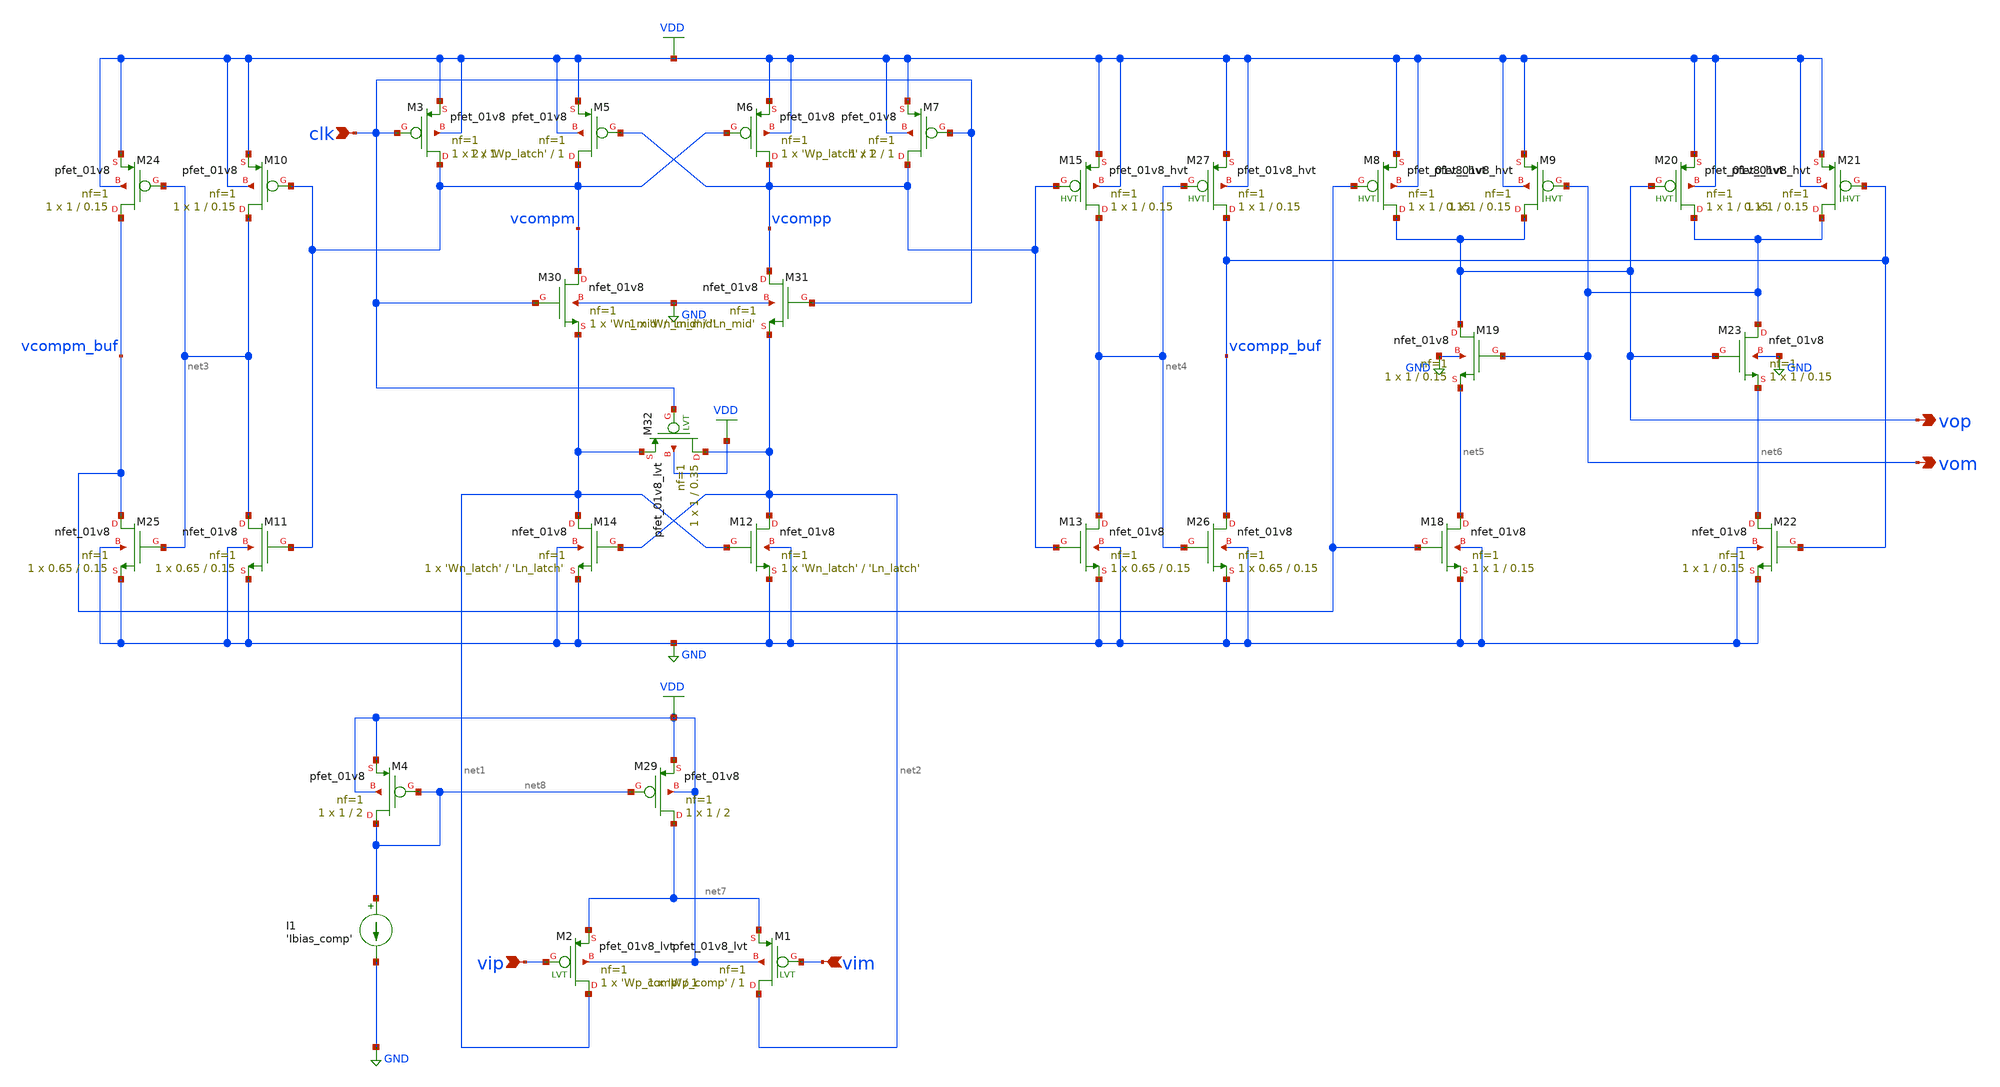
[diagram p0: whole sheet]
** sch_path: designs/latched_comparator_folded.sch
**.subckt latched_comparator_folded vip vim vop vom clk
*.ipin vip
*.ipin vim
*.opin vop
*.opin vom
*.ipin clk
XM5 vcompm vcompp VDD VDD sky130_fd_pr__pfet_01v8 L=1 W='Wp_latch' nf=1 ad='int((nf+1)/2) * W/nf * 0.29'
+ as='int((nf+2)/2) * W/nf * 0.29' pd='2*int((nf+1)/2) * (W/nf + 0.29)' ps='2*int((nf+2)/2) * (W/nf + 0.29)'
+ nrd='0.29 / W' nrs='0.29 / W' sa=0 sb=0 sd=0 mult=1 m=1
XM10 net3 vcompm VDD VDD sky130_fd_pr__pfet_01v8 L=0.15 W=1 nf=1 ad='int((nf+1)/2) * W/nf * 0.29' as='int((nf+2)/2) * W/nf * 0.29'
+ pd='2*int((nf+1)/2) * (W/nf + 0.29)' ps='2*int((nf+2)/2) * (W/nf + 0.29)' nrd='0.29 / W' nrs='0.29 / W'
+ sa=0 sb=0 sd=0 mult=1 m=1
XM11 net3 vcompm GND GND sky130_fd_pr__nfet_01v8 L=0.15 W=0.65 nf=1 ad='int((nf+1)/2) * W/nf * 0.29'
+ as='int((nf+2)/2) * W/nf * 0.29' pd='2*int((nf+1)/2) * (W/nf + 0.29)' ps='2*int((nf+2)/2) * (W/nf + 0.29)'
+ nrd='0.29 / W' nrs='0.29 / W' sa=0 sb=0 sd=0 mult=1 m=1
XM13 net4 vcompp GND GND sky130_fd_pr__nfet_01v8 L=0.15 W=0.65 nf=1 ad='int((nf+1)/2) * W/nf * 0.29'
+ as='int((nf+2)/2) * W/nf * 0.29' pd='2*int((nf+1)/2) * (W/nf + 0.29)' ps='2*int((nf+2)/2) * (W/nf + 0.29)'
+ nrd='0.29 / W' nrs='0.29 / W' sa=0 sb=0 sd=0 mult=1 m=1
XM15 net4 vcompp VDD VDD sky130_fd_pr__pfet_01v8_hvt L=0.15 W=1 nf=1 ad='int((nf+1)/2) * W/nf * 0.29'
+ as='int((nf+2)/2) * W/nf * 0.29' pd='2*int((nf+1)/2) * (W/nf + 0.29)' ps='2*int((nf+2)/2) * (W/nf + 0.29)'
+ nrd='0.29 / W' nrs='0.29 / W' sa=0 sb=0 sd=0 mult=1 m=1
XM6 vcompp vcompm VDD VDD sky130_fd_pr__pfet_01v8 L=1 W='Wp_latch' nf=1 ad='int((nf+1)/2) * W/nf * 0.29'
+ as='int((nf+2)/2) * W/nf * 0.29' pd='2*int((nf+1)/2) * (W/nf + 0.29)' ps='2*int((nf+2)/2) * (W/nf + 0.29)'
+ nrd='0.29 / W' nrs='0.29 / W' sa=0 sb=0 sd=0 mult=1 m=1
XM12 net2 net1 GND GND sky130_fd_pr__nfet_01v8 L='Ln_latch' W='Wn_latch' nf=1 ad='int((nf+1)/2) * W/nf * 0.29'
+ as='int((nf+2)/2) * W/nf * 0.29' pd='2*int((nf+1)/2) * (W/nf + 0.29)' ps='2*int((nf+2)/2) * (W/nf + 0.29)'
+ nrd='0.29 / W' nrs='0.29 / W' sa=0 sb=0 sd=0 mult=1 m=1
XM14 net1 net2 GND GND sky130_fd_pr__nfet_01v8 L='Ln_latch' W='Wn_latch' nf=1 ad='int((nf+1)/2) * W/nf * 0.29'
+ as='int((nf+2)/2) * W/nf * 0.29' pd='2*int((nf+1)/2) * (W/nf + 0.29)' ps='2*int((nf+2)/2) * (W/nf + 0.29)'
+ nrd='0.29 / W' nrs='0.29 / W' sa=0 sb=0 sd=0 mult=1 m=1
XM3 vcompm clk VDD VDD sky130_fd_pr__pfet_01v8 L=1 W=2 nf=1 ad='int((nf+1)/2) * W/nf * 0.29' as='int((nf+2)/2) * W/nf * 0.29'
+ pd='2*int((nf+1)/2) * (W/nf + 0.29)' ps='2*int((nf+2)/2) * (W/nf + 0.29)' nrd='0.29 / W' nrs='0.29 / W'
+ sa=0 sb=0 sd=0 mult=1 m=1
XM7 vcompp clk VDD VDD sky130_fd_pr__pfet_01v8 L=1 W=2 nf=1 ad='int((nf+1)/2) * W/nf * 0.29' as='int((nf+2)/2) * W/nf * 0.29'
+ pd='2*int((nf+1)/2) * (W/nf + 0.29)' ps='2*int((nf+2)/2) * (W/nf + 0.29)' nrd='0.29 / W' nrs='0.29 / W'
+ sa=0 sb=0 sd=0 mult=1 m=1
XM8 vop vcompm_buf VDD VDD sky130_fd_pr__pfet_01v8_hvt L=0.15 W=1 nf=1 ad='int((nf+1)/2) * W/nf * 0.29'
+ as='int((nf+2)/2) * W/nf * 0.29' pd='2*int((nf+1)/2) * (W/nf + 0.29)' ps='2*int((nf+2)/2) * (W/nf + 0.29)'
+ nrd='0.29 / W' nrs='0.29 / W' sa=0 sb=0 sd=0 mult=1 m=1
XM9 vop vom VDD VDD sky130_fd_pr__pfet_01v8_hvt L=0.15 W=1 nf=1 ad='int((nf+1)/2) * W/nf * 0.29' as='int((nf+2)/2) * W/nf * 0.29'
+ pd='2*int((nf+1)/2) * (W/nf + 0.29)' ps='2*int((nf+2)/2) * (W/nf + 0.29)' nrd='0.29 / W' nrs='0.29 / W'
+ sa=0 sb=0 sd=0 mult=1 m=1
XM18 net5 vcompm_buf GND GND sky130_fd_pr__nfet_01v8 L=0.15 W=1 nf=1 ad='int((nf+1)/2) * W/nf * 0.29'
+ as='int((nf+2)/2) * W/nf * 0.29' pd='2*int((nf+1)/2) * (W/nf + 0.29)' ps='2*int((nf+2)/2) * (W/nf + 0.29)'
+ nrd='0.29 / W' nrs='0.29 / W' sa=0 sb=0 sd=0 mult=1 m=1
XM19 vop vom net5 GND sky130_fd_pr__nfet_01v8 L=0.15 W=1 nf=1 ad='int((nf+1)/2) * W/nf * 0.29' as='int((nf+2)/2) * W/nf * 0.29'
+ pd='2*int((nf+1)/2) * (W/nf + 0.29)' ps='2*int((nf+2)/2) * (W/nf + 0.29)' nrd='0.29 / W' nrs='0.29 / W'
+ sa=0 sb=0 sd=0 mult=1 m=1
XM20 vom vop VDD VDD sky130_fd_pr__pfet_01v8_hvt L=0.15 W=1 nf=1 ad='int((nf+1)/2) * W/nf * 0.29' as='int((nf+2)/2) * W/nf * 0.29'
+ pd='2*int((nf+1)/2) * (W/nf + 0.29)' ps='2*int((nf+2)/2) * (W/nf + 0.29)' nrd='0.29 / W' nrs='0.29 / W'
+ sa=0 sb=0 sd=0 mult=1 m=1
XM21 vom vcompp_buf VDD VDD sky130_fd_pr__pfet_01v8_hvt L=0.15 W=1 nf=1 ad='int((nf+1)/2) * W/nf * 0.29'
+ as='int((nf+2)/2) * W/nf * 0.29' pd='2*int((nf+1)/2) * (W/nf + 0.29)' ps='2*int((nf+2)/2) * (W/nf + 0.29)'
+ nrd='0.29 / W' nrs='0.29 / W' sa=0 sb=0 sd=0 mult=1 m=1
XM22 net6 vcompp_buf GND GND sky130_fd_pr__nfet_01v8 L=0.15 W=1 nf=1 ad='int((nf+1)/2) * W/nf * 0.29'
+ as='int((nf+2)/2) * W/nf * 0.29' pd='2*int((nf+1)/2) * (W/nf + 0.29)' ps='2*int((nf+2)/2) * (W/nf + 0.29)'
+ nrd='0.29 / W' nrs='0.29 / W' sa=0 sb=0 sd=0 mult=1 m=1
XM23 vom vop net6 GND sky130_fd_pr__nfet_01v8 L=0.15 W=1 nf=1 ad='int((nf+1)/2) * W/nf * 0.29' as='int((nf+2)/2) * W/nf * 0.29'
+ pd='2*int((nf+1)/2) * (W/nf + 0.29)' ps='2*int((nf+2)/2) * (W/nf + 0.29)' nrd='0.29 / W' nrs='0.29 / W'
+ sa=0 sb=0 sd=0 mult=1 m=1
XM24 vcompm_buf net3 VDD VDD sky130_fd_pr__pfet_01v8 L=0.15 W=1 nf=1 ad='int((nf+1)/2) * W/nf * 0.29'
+ as='int((nf+2)/2) * W/nf * 0.29' pd='2*int((nf+1)/2) * (W/nf + 0.29)' ps='2*int((nf+2)/2) * (W/nf + 0.29)'
+ nrd='0.29 / W' nrs='0.29 / W' sa=0 sb=0 sd=0 mult=1 m=1
XM25 vcompm_buf net3 GND GND sky130_fd_pr__nfet_01v8 L=0.15 W=0.65 nf=1 ad='int((nf+1)/2) * W/nf * 0.29'
+ as='int((nf+2)/2) * W/nf * 0.29' pd='2*int((nf+1)/2) * (W/nf + 0.29)' ps='2*int((nf+2)/2) * (W/nf + 0.29)'
+ nrd='0.29 / W' nrs='0.29 / W' sa=0 sb=0 sd=0 mult=1 m=1
XM26 vcompp_buf net4 GND GND sky130_fd_pr__nfet_01v8 L=0.15 W=0.65 nf=1 ad='int((nf+1)/2) * W/nf * 0.29'
+ as='int((nf+2)/2) * W/nf * 0.29' pd='2*int((nf+1)/2) * (W/nf + 0.29)' ps='2*int((nf+2)/2) * (W/nf + 0.29)'
+ nrd='0.29 / W' nrs='0.29 / W' sa=0 sb=0 sd=0 mult=1 m=1
XM27 vcompp_buf net4 VDD VDD sky130_fd_pr__pfet_01v8_hvt L=0.15 W=1 nf=1 ad='int((nf+1)/2) * W/nf * 0.29'
+ as='int((nf+2)/2) * W/nf * 0.29' pd='2*int((nf+1)/2) * (W/nf + 0.29)' ps='2*int((nf+2)/2) * (W/nf + 0.29)'
+ nrd='0.29 / W' nrs='0.29 / W' sa=0 sb=0 sd=0 mult=1 m=1
I1 net8 GND 'Ibias_comp'
XM4 net8 net8 VDD VDD sky130_fd_pr__pfet_01v8 L=2 W=1 nf=1 ad='int((nf+1)/2) * W/nf * 0.29' as='int((nf+2)/2) * W/nf * 0.29'
+ pd='2*int((nf+1)/2) * (W/nf + 0.29)' ps='2*int((nf+2)/2) * (W/nf + 0.29)' nrd='0.29 / W' nrs='0.29 / W'
+ sa=0 sb=0 sd=0 mult=1 m=1
XM29 net7 net8 VDD VDD sky130_fd_pr__pfet_01v8 L=2 W=1 nf=1 ad='int((nf+1)/2) * W/nf * 0.29' as='int((nf+2)/2) * W/nf * 0.29'
+ pd='2*int((nf+1)/2) * (W/nf + 0.29)' ps='2*int((nf+2)/2) * (W/nf + 0.29)' nrd='0.29 / W' nrs='0.29 / W'
+ sa=0 sb=0 sd=0 mult=1 m=1
XM2 net1 vip net7 VDD sky130_fd_pr__pfet_01v8_lvt L=1 W='Wp_comp' nf=1 ad='int((nf+1)/2) * W/nf * 0.29'
+ as='int((nf+2)/2) * W/nf * 0.29' pd='2*int((nf+1)/2) * (W/nf + 0.29)' ps='2*int((nf+2)/2) * (W/nf + 0.29)'
+ nrd='0.29 / W' nrs='0.29 / W' sa=0 sb=0 sd=0 mult=1 m=1
XM1 net2 vim net7 VDD sky130_fd_pr__pfet_01v8_lvt L=1 W='Wp_comp' nf=1 ad='int((nf+1)/2) * W/nf * 0.29'
+ as='int((nf+2)/2) * W/nf * 0.29' pd='2*int((nf+1)/2) * (W/nf + 0.29)' ps='2*int((nf+2)/2) * (W/nf + 0.29)'
+ nrd='0.29 / W' nrs='0.29 / W' sa=0 sb=0 sd=0 mult=1 m=1
XM30 vcompm clk net1 GND sky130_fd_pr__nfet_01v8 L='Ln_mid' W='Wn_mid' nf=1 ad='int((nf+1)/2) * W/nf * 0.29'
+ as='int((nf+2)/2) * W/nf * 0.29' pd='2*int((nf+1)/2) * (W/nf + 0.29)' ps='2*int((nf+2)/2) * (W/nf + 0.29)'
+ nrd='0.29 / W' nrs='0.29 / W' sa=0 sb=0 sd=0 mult=1 m=1
XM31 vcompp clk net2 GND sky130_fd_pr__nfet_01v8 L='Ln_mid' W='Wn_mid' nf=1 ad='int((nf+1)/2) * W/nf * 0.29'
+ as='int((nf+2)/2) * W/nf * 0.29' pd='2*int((nf+1)/2) * (W/nf + 0.29)' ps='2*int((nf+2)/2) * (W/nf + 0.29)'
+ nrd='0.29 / W' nrs='0.29 / W' sa=0 sb=0 sd=0 mult=1 m=1
XM32 net2 clk net1 VDD sky130_fd_pr__pfet_01v8_lvt L=0.35 W=1 nf=1 ad='int((nf+1)/2) * W/nf * 0.29' as='int((nf+2)/2) * W/nf * 0.29'
+ pd='2*int((nf+1)/2) * (W/nf + 0.29)' ps='2*int((nf+2)/2) * (W/nf + 0.29)' nrd='0.29 / W' nrs='0.29 / W'
+ sa=0 sb=0 sd=0 mult=1 m=1
**** begin user architecture code

.include $::SKYWATER_MODELS/cells/nfet_01v8/sky130_fd_pr__nfet_01v8__tt.corner.spice
.include $::SKYWATER_MODELS/cells/nfet_01v8_lvt/sky130_fd_pr__nfet_01v8_lvt__tt.corner.spice
.include $::SKYWATER_MODELS/cells/pfet_01v8/sky130_fd_pr__pfet_01v8__tt.corner.spice
.include $::SKYWATER_MODELS/cells/nfet_03v3_nvt/sky130_fd_pr__nfet_03v3_nvt__tt.corner.spice
.include $::SKYWATER_MODELS/cells/nfet_05v0_nvt/sky130_fd_pr__nfet_05v0_nvt__tt.corner.spice
.include $::SKYWATER_MODELS/cells/esd_nfet_01v8/sky130_fd_pr__esd_nfet_01v8__tt.corner.spice
.include $::SKYWATER_MODELS/cells/pfet_01v8_lvt/sky130_fd_pr__pfet_01v8_lvt__tt.corner.spice
.include $::SKYWATER_MODELS/cells/pfet_01v8_hvt/sky130_fd_pr__pfet_01v8_hvt__tt.corner.spice
.include $::SKYWATER_MODELS/cells/esd_pfet_g5v0d10v5/sky130_fd_pr__esd_pfet_g5v0d10v5__tt.corner.spice
.include $::SKYWATER_MODELS/cells/pfet_g5v0d10v5/sky130_fd_pr__pfet_g5v0d10v5__tt.corner.spice
.include $::SKYWATER_MODELS/cells/pfet_g5v0d16v0/sky130_fd_pr__pfet_g5v0d16v0__tt.corner.spice
.include $::SKYWATER_MODELS/cells/nfet_g5v0d10v5/sky130_fd_pr__nfet_g5v0d10v5__tt.corner.spice
.include $::SKYWATER_MODELS/cells/nfet_g5v0d16v0/sky130_fd_pr__nfet_g5v0d16v0__tt_discrete.corner.spice
.include $::SKYWATER_MODELS/cells/esd_nfet_g5v0d10v5/sky130_fd_pr__esd_nfet_g5v0d10v5__tt.corner.spice
.include $::SKYWATER_MODELS/models/corners/tt/nonfet.spice
* Mismatch parameters
.include $::SKYWATER_MODELS/cells/nfet_01v8/sky130_fd_pr__nfet_01v8__mismatch.corner.spice
.include $::SKYWATER_MODELS/cells/pfet_01v8/sky130_fd_pr__pfet_01v8__mismatch.corner.spice
.include $::SKYWATER_MODELS/cells/nfet_01v8_lvt/sky130_fd_pr__nfet_01v8_lvt__mismatch.corner.spice
.include $::SKYWATER_MODELS/cells/pfet_01v8_lvt/sky130_fd_pr__pfet_01v8_lvt__mismatch.corner.spice
.include $::SKYWATER_MODELS/cells/pfet_01v8_hvt/sky130_fd_pr__pfet_01v8_hvt__mismatch.corner.spice
.include $::SKYWATER_MODELS/cells/nfet_g5v0d10v5/sky130_fd_pr__nfet_g5v0d10v5__mismatch.corner.spice
.include $::SKYWATER_MODELS/cells/pfet_g5v0d10v5/sky130_fd_pr__pfet_g5v0d10v5__mismatch.corner.spice
.include $::SKYWATER_MODELS/cells/nfet_05v0_nvt/sky130_fd_pr__nfet_05v0_nvt__mismatch.corner.spice
.include $::SKYWATER_MODELS/cells/nfet_03v3_nvt/sky130_fd_pr__nfet_03v3_nvt__mismatch.corner.spice
* Resistor$::SKYWATER_MODELS/Capacitor
.include $::SKYWATER_MODELS/models/r+c/res_typical__cap_typical.spice
.include $::SKYWATER_MODELS/models/r+c/res_typical__cap_typical__lin.spice
* Special cells
.include $::SKYWATER_MODELS/models/corners/tt/specialized_cells.spice
* All models
.include $::SKYWATER_MODELS/models/all.spice
* Corner
.include $::SKYWATER_MODELS/models/corners/tt/rf.spice

**** end user architecture code
**.ends
.GLOBAL VDD
.GLOBAL GND
**** begin user architecture code

.include latched_comparator_folded_commands.spice

**** end user architecture code
.end
